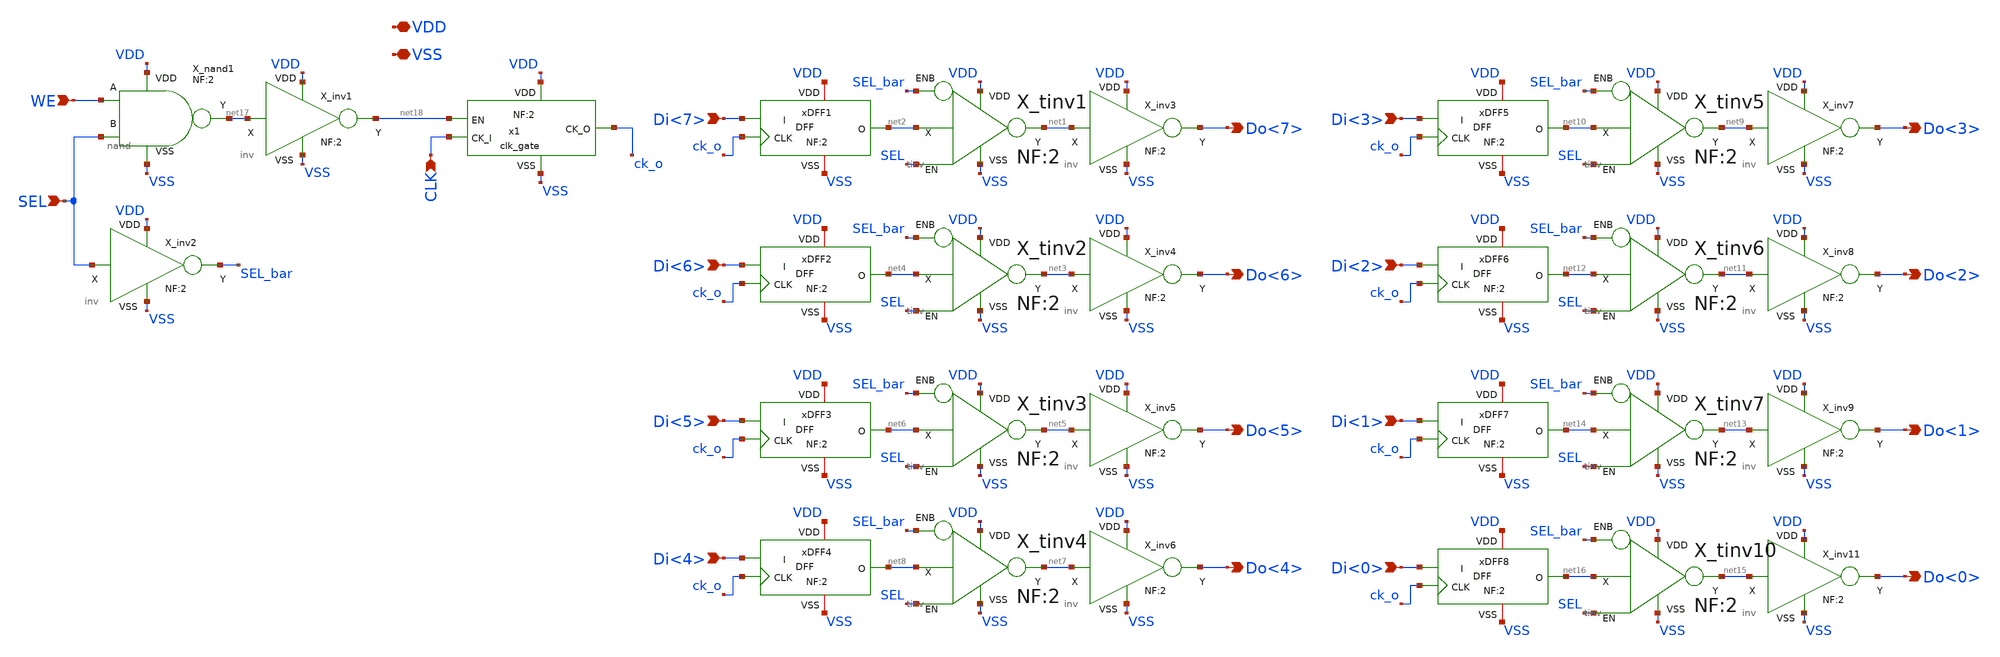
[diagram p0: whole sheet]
** sch_path: xschem_lib/sylee21/byte_dff.sch
**.subckt byte_dff Do<7> Di<7> Do<6> Di<6> Do<5> Di<5> Do<4> Di<4> Do<3> Di<3> Do<2> Di<2> Do<1>
*+ Di<1> Do<0> Di<0> WE SEL CLK VDD VSS
*.opin Do<7>
*.ipin Di<7>
*.opin Do<6>
*.ipin Di<6>
*.opin Do<5>
*.ipin Di<5>
*.opin Do<4>
*.ipin Di<4>
*.opin Do<3>
*.ipin Di<3>
*.opin Do<2>
*.ipin Di<2>
*.opin Do<1>
*.ipin Di<1>
*.opin Do<0>
*.ipin Di<0>
*.ipin WE
*.ipin SEL
*.ipin CLK
*.iopin VDD
*.iopin VSS
X_nand1 SEL WE net17 VDD VSS nand NF=2
X_inv1 net17 VDD VSS net18 inv NF=2
X_inv2 SEL VDD VSS SEL_bar inv NF=2
x1 VDD net18 ck_o CLK VSS clk_gate NF=2
xDFF1 VDD VSS Di<7> net2 ck_o DFF NF=2
X_tinv1 net2 SEL SEL_bar VDD VSS net1 tinv NF=2
X_inv3 net1 VDD VSS Do<7> inv NF=2
xDFF2 VDD VSS Di<6> net4 ck_o DFF NF=2
X_tinv2 net4 SEL SEL_bar VDD VSS net3 tinv NF=2
X_inv4 net3 VDD VSS Do<6> inv NF=2
xDFF3 VDD VSS Di<5> net6 ck_o DFF NF=2
X_tinv3 net6 SEL SEL_bar VDD VSS net5 tinv NF=2
X_inv5 net5 VDD VSS Do<5> inv NF=2
xDFF4 VDD VSS Di<4> net8 ck_o DFF NF=2
X_tinv4 net8 SEL SEL_bar VDD VSS net7 tinv NF=2
X_inv6 net7 VDD VSS Do<4> inv NF=2
xDFF5 VDD VSS Di<3> net10 ck_o DFF NF=2
X_tinv5 net10 SEL SEL_bar VDD VSS net9 tinv NF=2
X_inv7 net9 VDD VSS Do<3> inv NF=2
xDFF6 VDD VSS Di<2> net12 ck_o DFF NF=2
X_tinv6 net12 SEL SEL_bar VDD VSS net11 tinv NF=2
X_inv8 net11 VDD VSS Do<2> inv NF=2
xDFF7 VDD VSS Di<1> net14 ck_o DFF NF=2
X_tinv7 net14 SEL SEL_bar VDD VSS net13 tinv NF=2
X_inv9 net13 VDD VSS Do<1> inv NF=2
xDFF8 VDD VSS Di<0> net16 ck_o DFF NF=2
X_tinv10 net16 SEL SEL_bar VDD VSS net15 tinv NF=2
X_inv11 net15 VDD VSS Do<0> inv NF=2
**.ends
.end
